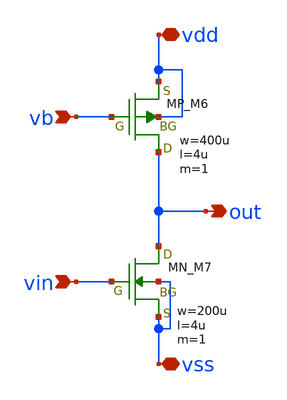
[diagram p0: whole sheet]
** sch_path: member_project/opamp/july_fifth/cs.sch
**.subckt cs vb vin out vss vdd
*.ipin vb
*.ipin vin
*.opin out
*.iopin vss
*.iopin vdd
XM6 out vb vdd vdd PMOS w=400u l=4u as=0 ad=0 ps=0 pd=0 nrd=0 nrs=0 m=1
XM7 out vin vss vss NMOS w=200u l=4u as=0 ad=0 ps=0 pd=0 nrd=0 nrs=0 m=1
**.ends
.end
